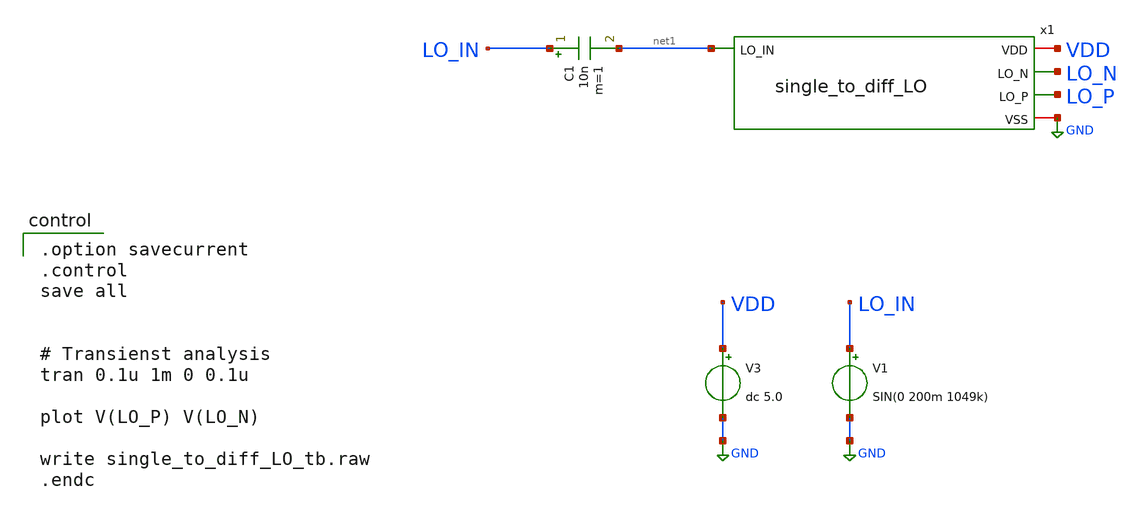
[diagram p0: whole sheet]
** sch_path: member_project/MIXER/noritsuna/xschem/single_to_diff_LO_tb.sch
**.subckt single_to_diff_LO_tb
x1 VDD LO_N net1 LO_P GND single_to_diff_LO
V3 VDD GND dc 5.0
C1 LO_IN net1 10n m=1
V1 LO_IN GND SIN(0 200m 1049k)
**** begin user architecture code
 .include $::LIB/ip62_models

.option savecurrent
.control
save all


# Transienst analysis
tran 0.1u 1m 0 0.1u

plot V(LO_P) V(LO_N)

write single_to_diff_LO_tb.raw
.endc

**** end user architecture code
**.ends

* expanding   symbol:  single_to_diff_LO.sym # of pins=5
** sym_path: member_project/MIXER/noritsuna/xschem/single_to_diff_LO.sym
** sch_path: member_project/MIXER/noritsuna/xschem/single_to_diff_LO.sch
.subckt single_to_diff_LO VDD LO_N LO_IN LO_P VSS
*.iopin VDD
*.iopin VSS
*.opin LO_N
*.opin LO_P
*.ipin LO_IN
XXM1 LO_N LO_IN LO_P VSS NMOS w=100u l=2u nrd=0 nrs=0 m=1
XR1 VDD LO_N VDD F_RR w=4.0e-06 l=15.8e-06 R=2.5e+03 tc1=0 tc2=0 m=1
XR2 LO_P VSS VDD F_RR w=4.0e-06 l=15.8e-06 R=2.5e+03 tc1=0 tc2=0 m=1
XR3 VDD LO_IN VDD F_RR w=2.8e-06 l=49.2e-06 R=20e+03 tc1=0 tc2=0 m=1
XR4 net1 VSS VDD F_RR w=2.8e-06 l=49.2e-06 R=40e+03 tc1=0 tc2=0 m=1
XXM6 LO_N VSS VSS VSS NMOS w=10u l=2u nrd=0 nrs=0 m=2
XR5 LO_IN net1 VDD F_RR w=2.8e-06 l=49.2e-06 R=40e+03 tc1=0 tc2=0 m=1
.ends

.GLOBAL GND
.end
